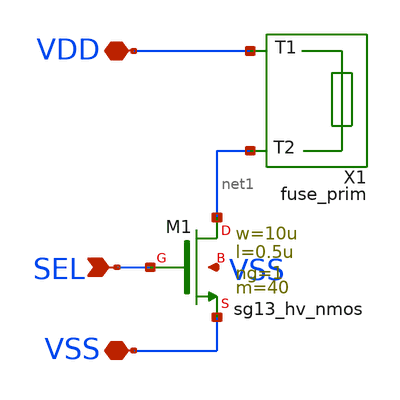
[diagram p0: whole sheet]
** sch_path: ip/util/xschem/fuse.sch
**.subckt fuse VSS VDD SEL
*.iopin VSS
*.iopin VDD
*.ipin SEL
XM1 net1 SEL VSS VSS sg13_hv_nmos w=10u l=0.5u ng=1 m=40 mm_ok=1
X1 VDD net1 fuse_prim
**.ends

* expanding   symbol:  fuse_prim.sym # of pins=2
** sym_path: ip/util/xschem/fuse_prim.sym
** sch_path: ip/util/xschem/fuse_prim.sch
.subckt fuse_prim T1 T2
*.iopin T2
*.iopin T1
R1 T1 T2 50 m=1
.ends

.end
